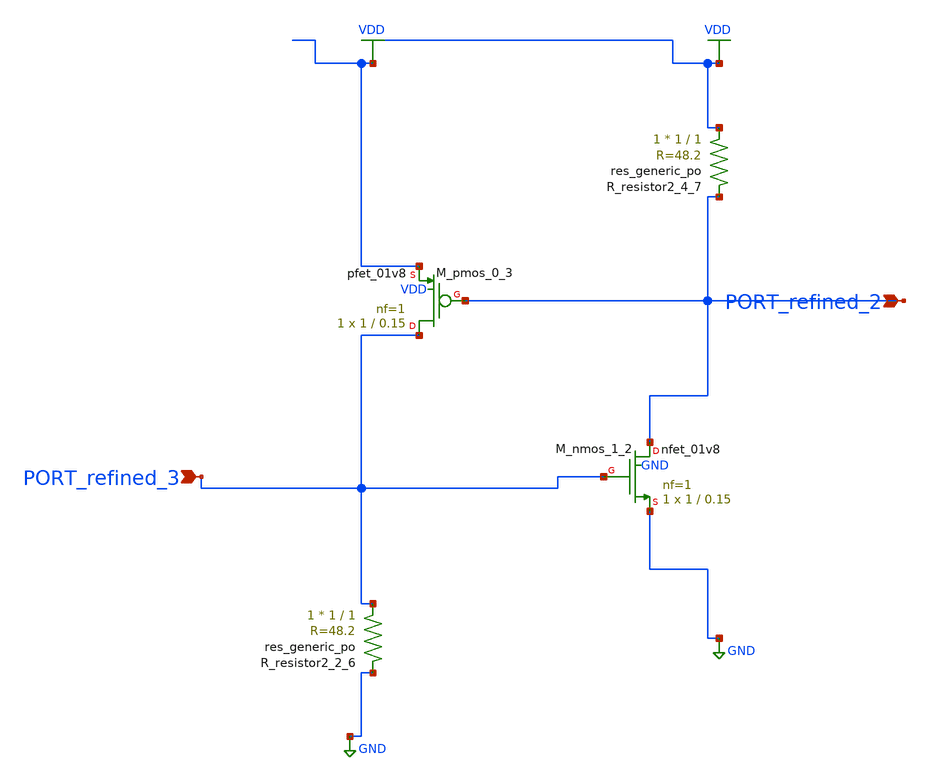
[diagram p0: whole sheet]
** sch_path: schematics/AMSNet/520.sch
**.subckt 520 PORT_refined_3 PORT_refined_2
*.ipin PORT_refined_3
*.ipin PORT_refined_2
XM_nmos_1_2 PORT_refined_2 PORT_refined_3 GND GND sky130_fd_pr__nfet_01v8 L=0.15 W=1 nf=1 ad='int((1 + 1)/2) * 1 / 1 * 0.29'
+ as='int((1 + 2)/2) * 1 / 1 * 0.29' pd='2*int((1 + 1)/2) * (1 / 1 + 0.29)' ps='2*int((1 + 2)/2) * (1 / 1 + 0.29)'
+ nrd='0.29 / 1 ' nrs='0.29 / 1 ' sa=0 sb=0 sd=0 mult=1 m=1
XM_pmos_0_3 PORT_refined_3 PORT_refined_2 VDD VDD sky130_fd_pr__pfet_01v8 L=0.15 W=1 nf=1 ad='int((1 + 1)/2) * 1 / 1 * 0.29'
+ as='int((1 + 2)/2) * 1 / 1 * 0.29' pd='2*int((1 + 1)/2) * (1 / 1 + 0.29)' ps='2*int((1 + 2)/2) * (1 / 1 + 0.29)'
+ nrd='0.29 / 1 ' nrs='0.29 / 1 ' sa=0 sb=0 sd=0 mult=1 m=1
XR_resistor2_2_6 PORT_refined_3 GND sky130_fd_pr__res_generic_po W=1 L=1 m=1
XR_resistor2_4_7 VDD PORT_refined_2 sky130_fd_pr__res_generic_po W=1 L=1 m=1
**.ends
.GLOBAL GND
.GLOBAL VDD
.end
